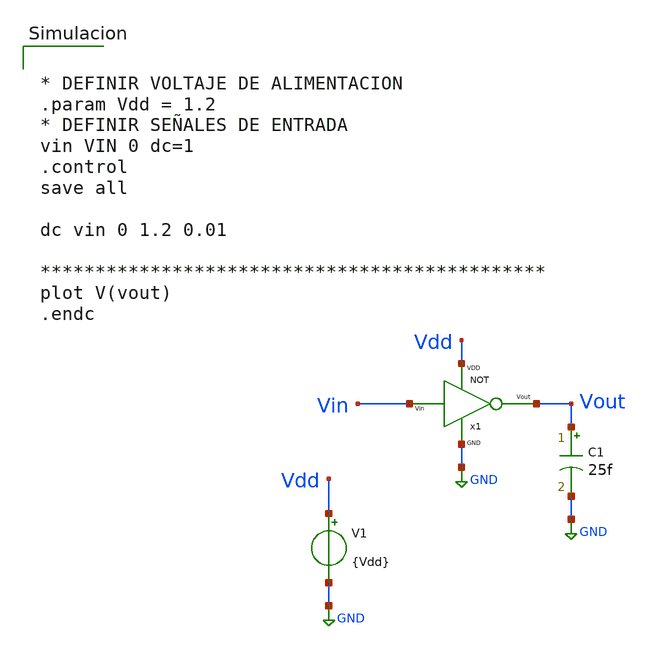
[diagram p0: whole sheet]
** sch_path: xschem/LogicGates/DC_NOT.sch
**.subckt DC_NOT
x1 Vdd Vin Vout GND NOT
V1 Vdd GND {Vdd}
C1 Vout GND 25f m=1
**** begin user architecture code


.lib cornerMOShv.lib mos_tt
.lib cornerMOSlv.lib mos_tt
*.lib cornerMOShv.lib mos_ff
*.lib cornerMOSlv.lib mos_ff
*.lib cornerMOShv.lib mos_ss
*.lib cornerMOSlv.lib mos_ss
*.lib cornerMOShv.lib mos_sf
*.lib cornerMOSlv.lib mos_sf
*.lib cornerMOShv.lib mos_fs
*.lib cornerMOSlv.lib mos_fs

*.include /opt/pdks/ihp-sg13g2/libs.ref/sg13g2_stdcell/spice/sg13g2_stdcell.spice
*.lib $::SG13G2_MODELS/cornerRES.lib res_typ
*.lib $::SG13G2_MODELS/cornerCAP.lib cap_typ
*.lib $::SG13G2_MODELS/diodes.lib



* DEFINIR VOLTAJE DE ALIMENTACION
.param Vdd = 1.2
* DEFINIR SEÑALES DE ENTRADA
vin VIN 0 dc=1
.control
save all

dc vin 0 1.2 0.01

**********************************************
plot V(vout)
.endc


**** end user architecture code
**.ends

* expanding   symbol:  ../LogicGates/NOT.sym # of pins=4
** sym_path: xschem/LogicGates/NOT.sym
** sch_path: xschem/LogicGates/NOT.sch
.subckt NOT VDD Vin Vout GND
*.ipin VDD
*.ipin Vin
*.ipin GND
*.opin Vout
XM3 GND Vin Vout GND sg13_hv_nmos w=10.0u l=5u ng=1 m=1 mm_ok=1
XM4 Vout Vin VDD VDD sg13_hv_pmos w=2.72u l=0.45u ng=1 m=1 mm_ok=1
.ends

.GLOBAL GND
.end
